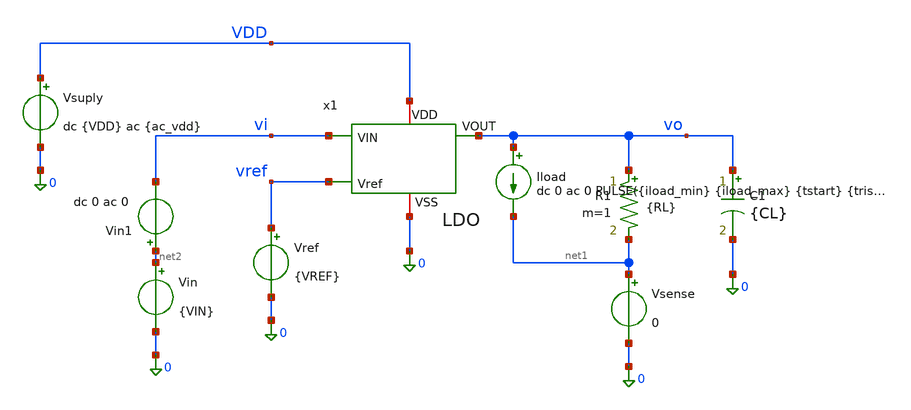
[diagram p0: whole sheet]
** sch_path: xschem/ldo_tb.sch
**.subckt ldo_tb
Vsuply VDD 0 dc {VDD} ac {ac_vdd}
Vref vref 0 {VREF}
Vin net2 0 {VIN}
R1 vo net1 {RL} m=1
C1 vo 0 {CL} m=1
Iload vo net1 dc 0 ac 0 PULSE({iload_min} {iload_max} {tstart} {trise} {tfall} {twidth} {tperiod})
Vsense net1 0 0
Vin1 net2 vi dc 0 ac 0
x1 vi vo VDD vref 0 LDO
**** begin user architecture code




* 1. Inclusión de libreria de modelos Sky130 PRIMERO
.lib /foss/pdks/sky130A/libs.tech/ngspice/sky130.lib.spice tt
.option temp=125
.option num_threads=8

**parametros_ldo
.param VDD = 1.8
.param VREF = 0.6
.param VIN = '1*VDD'
.param RL = 12
.param CL = 1u
.param tsim = 2m
* Parámetros para la prueba de carga del LDO
.param iload_min = 1m
.param iload_max = 50m
.param tstart   = 10u
.param trise    = 100n
.param tfall    = 100n
.param twidth   = 100u
.param tperiod  = 200u

.param tsim = '3*tperiod'

.param ac_iprobe = 1
.param ac_vdd = 0




.control
let tperiod  = 200u
let tsim = '3*tperiod'




* 1. Punto de Operación (.OP)

* --- Circuito de Polarización (Referencia) ---
save all


save @m.x1.xM1.msky130_fd_pr__pfet_01v8_lvt[gm]
save @m.x1.xM1.msky130_fd_pr__pfet_01v8_lvt[gds]
save @m.x1.xM1.msky130_fd_pr__pfet_01v8_lvt[id]
save @m.x1.xM1.msky130_fd_pr__pfet_01v8_lvt[vgs]
save @m.x1.xM1.msky130_fd_pr__pfet_01v8_lvt[vds]
save @m.x1.xM1.msky130_fd_pr__pfet_01v8_lvt[vth]
save @m.x1.xM1.msky130_fd_pr__pfet_01v8_lvt[vdsat]


* Mr1 (pfet_01v8_lvt)
save @m.x1.x1.xMr1.msky130_fd_pr__pfet_01v8_lvt[gm]
save @m.x1.x1.xMr1.msky130_fd_pr__pfet_01v8_lvt[gds]
save @m.x1.x1.xMr1.msky130_fd_pr__pfet_01v8_lvt[id]
save @m.x1.x1.xMr1.msky130_fd_pr__pfet_01v8_lvt[vgs]
save @m.x1.x1.xMr1.msky130_fd_pr__pfet_01v8_lvt[vds]
save @m.x1.x1.xMr1.msky130_fd_pr__pfet_01v8_lvt[vth]
save @m.x1.x1.xMr1.msky130_fd_pr__pfet_01v8_lvt[vdsat]

* Mr (pfet_01v8_lvt)
save @m.x1.x1.xMr.msky130_fd_pr__pfet_01v8_lvt[gm]
save @m.x1.x1.xMr.msky130_fd_pr__pfet_01v8_lvt[gds]
save @m.x1.x1.xMr.msky130_fd_pr__pfet_01v8_lvt[id]
save @m.x1.x1.xMr.msky130_fd_pr__pfet_01v8_lvt[vgs]
save @m.x1.x1.xMr.msky130_fd_pr__pfet_01v8_lvt[vds]
save @m.x1.x1.xMr.msky130_fd_pr__pfet_01v8_lvt[vth]
save @m.x1.x1.xMr.msky130_fd_pr__pfet_01v8_lvt[vdsat]

* Mp2 (nfet_01v8)
save @m.x1.x1.xMp2.msky130_fd_pr__nfet_01v8[gm]
save @m.x1.x1.xMp2.msky130_fd_pr__nfet_01v8[gds]
save @m.x1.x1.xMp2.msky130_fd_pr__nfet_01v8[id]
save @m.x1.x1.xMp2.msky130_fd_pr__nfet_01v8[vgs]
save @m.x1.x1.xMp2.msky130_fd_pr__nfet_01v8[vds]
save @m.x1.x1.xMp2.msky130_fd_pr__nfet_01v8[vth]
save @m.x1.x1.xMp2.msky130_fd_pr__nfet_01v8[vdsat]

* Mc3 (nfet_01v8)
save @m.x1.x1.xMc3.msky130_fd_pr__nfet_01v8[gm]
save @m.x1.x1.xMc3.msky130_fd_pr__nfet_01v8[gds]
save @m.x1.x1.xMc3.msky130_fd_pr__nfet_01v8[id]
save @m.x1.x1.xMc3.msky130_fd_pr__nfet_01v8[vgs]
save @m.x1.x1.xMc3.msky130_fd_pr__nfet_01v8[vds]
save @m.x1.x1.xMc3.msky130_fd_pr__nfet_01v8[vth]
save @m.x1.x1.xMc3.msky130_fd_pr__nfet_01v8[vdsat]


* --- Etapa Diferencial (Núcleo del OTA) ---

* Mrc1 (pfet_01v8_lvt)
save @m.x1.x1.xMrc1.msky130_fd_pr__pfet_01v8_lvt[gm]
save @m.x1.x1.xMrc1.msky130_fd_pr__pfet_01v8_lvt[gds]
save @m.x1.x1.xMrc1.msky130_fd_pr__pfet_01v8_lvt[id]
save @m.x1.x1.xMrc1.msky130_fd_pr__pfet_01v8_lvt[vgs]
save @m.x1.x1.xMrc1.msky130_fd_pr__pfet_01v8_lvt[vds]
save @m.x1.x1.xMrc1.msky130_fd_pr__pfet_01v8_lvt[vth]
save @m.x1.x1.xMrc1.msky130_fd_pr__pfet_01v8_lvt[vdsat]

* Mn (pfet_01v8)
save @m.x1.x1.xMn.msky130_fd_pr__pfet_01v8[gm]
save @m.x1.x1.xMn.msky130_fd_pr__pfet_01v8[gds]
save @m.x1.x1.xMn.msky130_fd_pr__pfet_01v8[id]
save @m.x1.x1.xMn.msky130_fd_pr__pfet_01v8[vgs]
save @m.x1.x1.xMn.msky130_fd_pr__pfet_01v8[vds]
save @m.x1.x1.xMn.msky130_fd_pr__pfet_01v8[vth]
save @m.x1.x1.xMn.msky130_fd_pr__pfet_01v8[vdsat]

* Mp (pfet_01v8)
save @m.x1.x1.xMp.msky130_fd_pr__pfet_01v8[gm]
save @m.x1.x1.xMp.msky130_fd_pr__pfet_01v8[gds]
save @m.x1.x1.xMp.msky130_fd_pr__pfet_01v8[id]
save @m.x1.x1.xMp.msky130_fd_pr__pfet_01v8[vgs]
save @m.x1.x1.xMp.msky130_fd_pr__pfet_01v8[vds]
save @m.x1.x1.xMp.msky130_fd_pr__pfet_01v8[vth]
save @m.x1.x1.xMp.msky130_fd_pr__pfet_01v8[vdsat]

* Mnr (nfet_01v8)
save @m.x1.x1.xMnr.msky130_fd_pr__nfet_01v8[gm]
save @m.x1.x1.xMnr.msky130_fd_pr__nfet_01v8[gds]
save @m.x1.x1.xMnr.msky130_fd_pr__nfet_01v8[id]
save @m.x1.x1.xMnr.msky130_fd_pr__nfet_01v8[vgs]
save @m.x1.x1.xMnr.msky130_fd_pr__nfet_01v8[vds]
save @m.x1.x1.xMnr.msky130_fd_pr__nfet_01v8[vth]
save @m.x1.x1.xMnr.msky130_fd_pr__nfet_01v8[vdsat]

* Mpr (nfet_01v8)
save @m.x1.x1.xMpr.msky130_fd_pr__nfet_01v8[gm]
save @m.x1.x1.xMpr.msky130_fd_pr__nfet_01v8[gds]
save @m.x1.x1.xMpr.msky130_fd_pr__nfet_01v8[id]
save @m.x1.x1.xMpr.msky130_fd_pr__nfet_01v8[vgs]
save @m.x1.x1.xMpr.msky130_fd_pr__nfet_01v8[vds]
save @m.x1.x1.xMpr.msky130_fd_pr__nfet_01v8[vth]
save @m.x1.x1.xMpr.msky130_fd_pr__nfet_01v8[vdsat]


* --- Etapa de Salida ---

* Mrc2 (pfet_01v8_lvt)
save @m.x1.x1.xMrc2.msky130_fd_pr__pfet_01v8_lvt[gm]
save @m.x1.x1.xMrc2.msky130_fd_pr__pfet_01v8_lvt[gds]
save @m.x1.x1.xMrc2.msky130_fd_pr__pfet_01v8_lvt[id]
save @m.x1.x1.xMrc2.msky130_fd_pr__pfet_01v8_lvt[vgs]
save @m.x1.x1.xMrc2.msky130_fd_pr__pfet_01v8_lvt[vds]
save @m.x1.x1.xMrc2.msky130_fd_pr__pfet_01v8_lvt[vth]
save @m.x1.x1.xMrc2.msky130_fd_pr__pfet_01v8_lvt[vdsat]

* Mo (nfet_01v8)
save @m.x1.x1.xMo.msky130_fd_pr__nfet_01v8[gm]
save @m.x1.x1.xMo.msky130_fd_pr__nfet_01v8[gds]
save @m.x1.x1.xMo.msky130_fd_pr__nfet_01v8[id]
save @m.x1.x1.xMo.msky130_fd_pr__nfet_01v8[vgs]
save @m.x1.x1.xMo.msky130_fd_pr__nfet_01v8[vds]
save @m.x1.x1.xMo.msky130_fd_pr__nfet_01v8[vth]
save @m.x1.x1.xMo.msky130_fd_pr__nfet_01v8[vdsat]


op
set filetype=ascii
write LDO_op.raw




* 2. Análisis Transitorio para overshot y undershot (.TRAN)
tran 1u $&tsim
write LDO_tran_picos.raw

* 3. Análisis en Frecuencia  para estabilidad (.AC)
alterparam ac_iprobe = 1
alterparam ac_vdd = 0
reset
ac dec 10 1 1G
* 1. Ganancia de Lazo Abierto T(s) = v(x1.vre) / v(x1.vre2)
let T_loop = v(x1.vre) / v(x1.vre2)
let ldb = vdb(T_loop)
let fase = vp(T_loop) * 180 / pi

write LDO_ac_estability.raw


* 5. Analisis en dc sweep para el line regulation
dc vin 1.3 1.74 0.05
*plot vo
*plot vi
write LDO_dc_line.raw

*6. análisis en Frecuencia (.AC) para el PSRR
alterparam ac_iprobe = 0
alterparam ac_vdd = 1
reset
ac dec 10 10 1G
* 1. Ganancia de Lazo Abierto T(s) = v(x1.vre) / v(x1.net3)
let psrr1 = v(vdd)/v(vo)
let psrr_db = vdb(psrr1)
write LDO_ac_psrr.raw

* 4. Análisis en dc sweep para el load regulation
alterparam RL = 100
reset
dc iload 1m 10m 100u
*plot vo
*plot vsense#branch
write LDO_dc_load.raw


* ANALISIS EN DC PARA EL DROPOUT
alterparam RL = 24
reset
dc vin1 0 2 0.05
write LDO_dc_dropout.raw




*CALCULOS PARA ESTABILIDAD Y GANANCIA EN LAZO ABIERTO

setplot ac1
* 2. UGB (Frecuencia donde la magnitud cruza 0 dB)
meas ac ugb WHEN ldb = 0.0
* 3. Medir la fase en grados en el punto exacto del UGB
meas ac fase_ugb FIND fase WHEN ldb = 0.0

* 4. Calcular el Margen de Fase (PM = fase_ugb)
let margen_fase = fase
meas ac ganancia_banda_plana   find ldb at=1
echo 'margen_fase = $&fase_ugb'

*CALCULOS PARA EL PSRR
setplot ac2
meas ac gananciaPSRR_1   find psrr_db at=1
meas ac gananciaPSRR_1k  find psrr_db at=1k
meas ac gananciaPSRR_10k find psrr_db at=10k
meas ac gananciaPSRR_1M  find psrr_db at=1Meg

*CALCULOS PARA EL LOAD REGULATION
setplot dc1
meas dc voload_max MAX v(vo)
meas dc voload_min MIN v(vo)
let load_regulation = voload_max - voload_min
echo 'load_regulation = $&load_regulation'

*CALCULOS PARA EL LINE REGULATION
setplot dc2
meas dc voline_max MAX v(vo)
meas dc voline_min MIN v(vo)
let line_regulation = voline_max - voline_min
echo 'line_regulation = $&line_regulation'

*CALCULOS PARA EL DROPOUT
setplot dc3

* 1. Usamos v(vo) para el nodo y v-sweep para el eje X (que es el barrido de 'vin')
meas dc vout_nom FIND v(vo) WHEN vi = 1.55

* 2. Calcular dinámicamente el valor objetivo al 99.5% (0.5% de caída según tu código)
let vout_target = vout_nom * 0.995

* 3. Encontrar el Vin en el que Vout cruza el vout_target (usamos cross=1 en lugar de fall=1)
meas dc vin_do FIND vi WHEN vo = vout_target fall=1

* 4. Calcular el Dropout exacto (cambiado *e3 por *1e3)
let dropout_mV = (vin_do - vout_target) * 1e3

* 5. Imprimir las variables con los nombres correctos
print vout_nom vout_target vin_do dropout_mV

*CALCULOS PARA OVERSHOOT E UNDERSHOOT
*CALCULOS PARA OVERSHOOT E UNDERSHOOT
setplot tran1

* 1. Medir el voltaje estable en carga ligera (justo antes de tstart = 10u)
meas tran v_estable_ligera FIND v(vo) AT=9u

* 2. Medir el voltaje estable en carga pesada (justo antes de que acabe el pulso en 210u)
meas tran v_estable_pesada FIND v(vo) AT=20u

* 3. Encontrar los picos absolutos de la simulación
meas tran vo_max MAX v(vo)
meas tran vo_min MIN v(vo)

* 4. Calcular el Undershoot y Overshoot verdaderos (en milivoltios)
* Undershoot: Lo que cae respecto al valor que tenía en carga ligera
let undershoot_mV = (v_estable_ligera - vo_min) * 1e3

* Overshoot: Lo que sube respecto al valor que tenía en carga pesada
let overshoot_mV = (vo_max - v_estable_pesada) * 1e3

* 5. Imprimir resultados en la consola
echo '--- RESULTADOS DE TRANSIENTE ---'
print undershoot_mV overshoot_mV v_estable_ligera v_estable_pesada
.endc



**** end user architecture code
**.ends

* expanding   symbol:  /foss/designs/LDO-sky130/xschem/LDO.sym # of pins=5
** sym_path: xschem/LDO.sym
** sch_path: xschem/LDO.sch
.subckt LDO VIN VOUT VDD Vref VSS
*.ipin VIN
*.iopin VDD
*.opin VOUT
*.ipin Vref
*.iopin VSS
XR1 Vre VOUT VSS sky130_fd_pr__res_iso_pw W=0.35 L=10.17 m=1
XR2 VSS Vre VSS sky130_fd_pr__res_iso_pw W=0.35 L=10 m=1
V1 vre2 Vre 0 ac {ac_iprobe}
XC1 VOUT Vre sky130_fd_pr__cap_mim_m3_2 W=19.5 L=19.5 MF=1 m=1
XC2 VOUT VSS sky130_fd_pr__cap_mim_m3_2 W=40 L=40 MF=1 m=1
x1 VDD Vgp Vref vre2 VSS OTA
XM2 VOUT Vgp VIN VDD sky130_fd_pr__pfet_01v8 L=0.5 W=1000 nf=100 ad='int((100 + 1)/2) * 1000 / 100 * 0.29'
+ as='int((100 + 2)/2) * 1000 / 100 * 0.29' pd='2*int((100 + 1)/2) * (1000 / 100 + 0.29)' ps='2*int((100 + 2)/2) * (1000 / 100 + 0.29)'
+ nrd='0.29 / 1000 ' nrs='0.29 / 1000 ' sa=0 sb=0 sd=0 mult=5 m=5
.ends


* expanding   symbol:  /foss/designs/LDO-sky130/xschem/OTA.sym # of pins=5
** sym_path: xschem/OTA.sym
** sch_path: xschem/OTA.sch
.subckt OTA VDD VO_ota VIN_ota VIP_ota VSS
*.ipin VIN_ota
*.opin VO_ota
*.iopin VSS
*.iopin VDD
*.ipin VIP_ota
XR1 VO_ota1 net1 VDD sky130_fd_pr__res_high_po W=0.35 L=360 mult=1 m=1
XC1 VO_ota net1 sky130_fd_pr__cap_mim_m3_2 W=50 L=50 MF=1 m=1
XMpr VO_ota1 vd VSS VSS sky130_fd_pr__nfet_01v8 L=0.5 W=3 nf=1 ad='int((1 + 1)/2) * 3 / 1 * 0.29' as='int((1 + 2)/2) * 3 / 1 * 0.29'
+ pd='2*int((1 + 1)/2) * (3 / 1 + 0.29)' ps='2*int((1 + 2)/2) * (3 / 1 + 0.29)' nrd='0.29 / 3 ' nrs='0.29 / 3 '
+ sa=0 sb=0 sd=0 mult=1 m=1
XMnr vd vd VSS VSS sky130_fd_pr__nfet_01v8 L=0.5 W=3 nf=1 ad='int((1 + 1)/2) * 3 / 1 * 0.29' as='int((1 + 2)/2) * 3 / 1 * 0.29'
+ pd='2*int((1 + 1)/2) * (3 / 1 + 0.29)' ps='2*int((1 + 2)/2) * (3 / 1 + 0.29)' nrd='0.29 / 3 ' nrs='0.29 / 3 '
+ sa=0 sb=0 sd=0 mult=1 m=1
XMn vd VIN_ota Vtail VDD sky130_fd_pr__pfet_01v8 L=0.5 W=28 nf=1 ad='int((1 + 1)/2) * 28 / 1 * 0.29'
+ as='int((1 + 2)/2) * 28 / 1 * 0.29' pd='2*int((1 + 1)/2) * (28 / 1 + 0.29)' ps='2*int((1 + 2)/2) * (28 / 1 + 0.29)'
+ nrd='0.29 / 28 ' nrs='0.29 / 28 ' sa=0 sb=0 sd=0 mult=1 m=1
XMp VO_ota1 VIP_ota Vtail VDD sky130_fd_pr__pfet_01v8 L=0.5 W=28 nf=1 ad='int((1 + 1)/2) * 28 / 1 * 0.29'
+ as='int((1 + 2)/2) * 28 / 1 * 0.29' pd='2*int((1 + 1)/2) * (28 / 1 + 0.29)' ps='2*int((1 + 2)/2) * (28 / 1 + 0.29)'
+ nrd='0.29 / 28 ' nrs='0.29 / 28 ' sa=0 sb=0 sd=0 mult=1 m=1
XMo VO_ota VO_ota1 VSS VSS sky130_fd_pr__nfet_01v8 L=0.5 W=3 nf=1 ad='int((1 + 1)/2) * 3 / 1 * 0.29'
+ as='int((1 + 2)/2) * 3 / 1 * 0.29' pd='2*int((1 + 1)/2) * (3 / 1 + 0.29)' ps='2*int((1 + 2)/2) * (3 / 1 + 0.29)'
+ nrd='0.29 / 3 ' nrs='0.29 / 3 ' sa=0 sb=0 sd=0 mult=1 m=1
XMrc1 Vtail VGP VDD VDD sky130_fd_pr__pfet_01v8_lvt L=0.5 W=40 nf=1 ad='int((1 + 1)/2) * 40 / 1 * 0.29'
+ as='int((1 + 2)/2) * 40 / 1 * 0.29' pd='2*int((1 + 1)/2) * (40 / 1 + 0.29)' ps='2*int((1 + 2)/2) * (40 / 1 + 0.29)'
+ nrd='0.29 / 40 ' nrs='0.29 / 40 ' sa=0 sb=0 sd=0 mult=1 m=1
XMrc2 VO_ota VGP VDD VDD sky130_fd_pr__pfet_01v8_lvt L=0.5 W=8 nf=1 ad='int((1 + 1)/2) * 8 / 1 * 0.29'
+ as='int((1 + 2)/2) * 8 / 1 * 0.29' pd='2*int((1 + 1)/2) * (8 / 1 + 0.29)' ps='2*int((1 + 2)/2) * (8 / 1 + 0.29)'
+ nrd='0.29 / 8 ' nrs='0.29 / 8 ' sa=0 sb=0 sd=0 mult=1 m=1
XMc3 VGP Viref rs VSS sky130_fd_pr__nfet_01v8 L=1 W=20 nf=1 ad='int((1 + 1)/2) * 20 / 1 * 0.29' as='int((1 + 2)/2) * 20 / 1 * 0.29'
+ pd='2*int((1 + 1)/2) * (20 / 1 + 0.29)' ps='2*int((1 + 2)/2) * (20 / 1 + 0.29)' nrd='0.29 / 20 ' nrs='0.29 / 20 '
+ sa=0 sb=0 sd=0 mult=1 m=1
XMp2 Viref Viref VSS VSS sky130_fd_pr__nfet_01v8 L=1 W=5 nf=1 ad='int((1 + 1)/2) * 5 / 1 * 0.29' as='int((1 + 2)/2) * 5 / 1 * 0.29'
+ pd='2*int((1 + 1)/2) * (5 / 1 + 0.29)' ps='2*int((1 + 2)/2) * (5 / 1 + 0.29)' nrd='0.29 / 5 ' nrs='0.29 / 5 '
+ sa=0 sb=0 sd=0 mult=1 m=1
XMr VGP VGP VDD VDD sky130_fd_pr__pfet_01v8_lvt L=0.5 W=2.4 nf=1 ad='int((1 + 1)/2) * 2.4 / 1 * 0.29'
+ as='int((1 + 2)/2) * 2.4 / 1 * 0.29' pd='2*int((1 + 1)/2) * (2.4 / 1 + 0.29)' ps='2*int((1 + 2)/2) * (2.4 / 1 + 0.29)'
+ nrd='0.29 / 2.4 ' nrs='0.29 / 2.4 ' sa=0 sb=0 sd=0 mult=1 m=1
XMr1 Viref VGP VDD VDD sky130_fd_pr__pfet_01v8_lvt L=1 W=8 nf=1 ad='int((1 + 1)/2) * 8 / 1 * 0.29' as='int((1 + 2)/2) * 8 / 1 * 0.29'
+ pd='2*int((1 + 1)/2) * (8 / 1 + 0.29)' ps='2*int((1 + 2)/2) * (8 / 1 + 0.29)' nrd='0.29 / 8 ' nrs='0.29 / 8 '
+ sa=0 sb=0 sd=0 mult=1 m=1
XRs VSS rs VSS sky130_fd_pr__res_iso_pw W=0.425 L=0.35 m=1
.ends

.end
